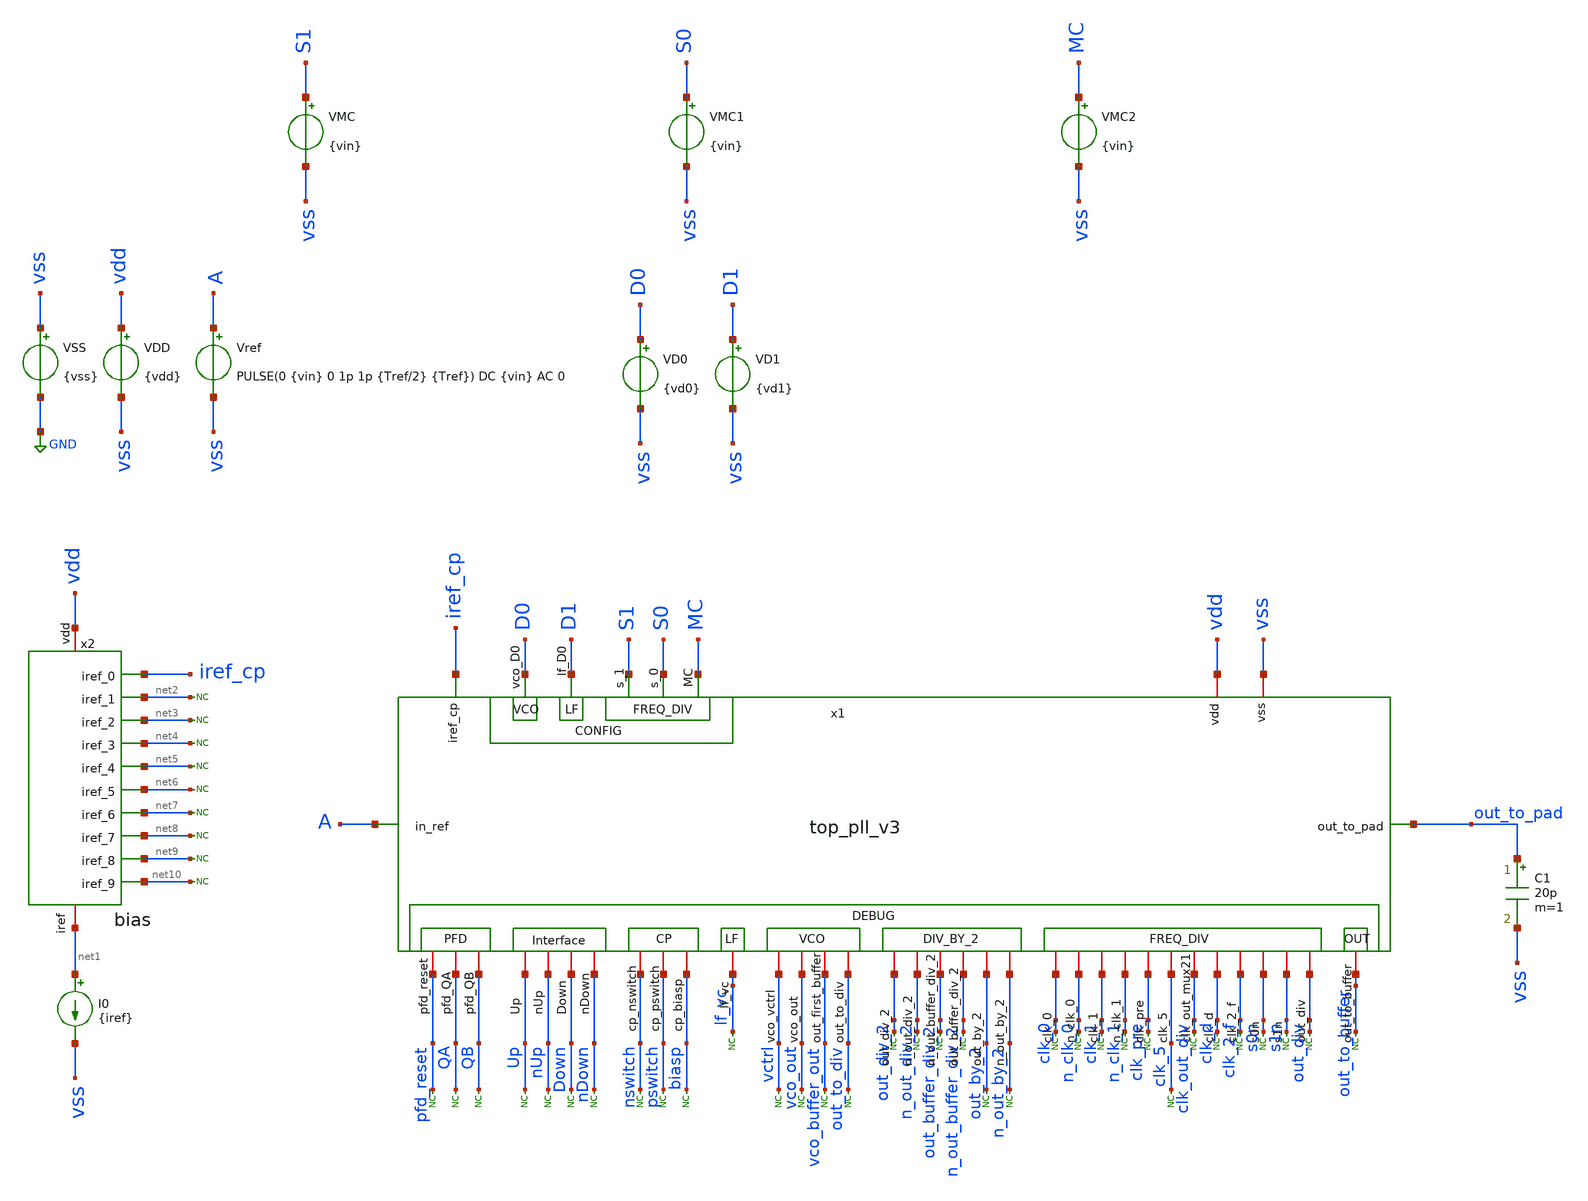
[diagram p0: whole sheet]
** sch_path: xschem/tb_top_pll_v3.sch
**.subckt tb_top_pll_v3
VSS vss GND {vss}
VDD vdd vss {vdd}
Vref A vss PULSE(0 {vin} 0 1p 1p {Tref/2} {Tref}) DC {vin} AC 0
VD0 D0 vss {vd0}
I0 net1 vss {iref}
* noconn #net2
* noconn #net3
* noconn #net4
* noconn #net5
* noconn #net6
* noconn #net7
* noconn #net8
* noconn #net9
* noconn #net10
* noconn clk_pre
* noconn n_clk_1
* noconn clk_1
* noconn n_clk_0
* noconn clk_0
* noconn n_out_buffer_div_2
* noconn out_buffer_div_2
* noconn n_out_div_2
* noconn out_div_2
* noconn nswitch
* noconn pswitch
* noconn biasp
* noconn pfd_reset
* noconn QA
* noconn QB
* noconn Up
* noconn nUp
* noconn Down
* noconn nDown
* noconn lf_vc
* noconn vctrl
* noconn vco_out
* noconn vco_buffer_out
* noconn out_to_div
* noconn out_by_2
* noconn n_out_by_2
* noconn clk_5
x2 vdd net1 iref_cp net2 net3 net4 net5 net6 net7 net8 net9 net10 bias
C1 out_to_pad vss 20p m=1
* noconn out_to_buffer
x1 iref_cp vss vdd vco_out vctrl Up QA out_to_buffer A nUp out_to_pad Down nDown QB D0 lf_vc
+ vco_buffer_out biasp pswitch nswitch pfd_reset S0 MC S1 out_by_2 out_to_div out_div n_out_by_2 n_out_div_2
+ out_div_2 out_buffer_div_2 n_out_buffer_div_2 n_clk_0 s1n s0n clk_2_f clk_d clk_out_div clk_5 clk_pre n_clk_1
+ clk_1 clk_0 D1 top_pll_v3
* noconn clk_out_div
* noconn clk_d
* noconn clk_2_f
* noconn s0n
* noconn s1n
* noconn out_div
VD1 D1 vss {vd1}
VMC S1 vss {vin}
VMC1 S0 vss {vin}
VMC2 MC vss {vin}
**** begin user architecture code



* Parameters
.param kp = 1.0
.param vdd = kp*1.8
.param vss = 0.0
.param vin = vdd
.param fref = 100e6
.param Tref = 1/fref
.param iref = 100u
.param vd0 = 0.0
.param vd1 = 0.0

.options TEMP = 100.0
.options RSHUNT = 1e20
.options GMIN = 1e-10

* Models
.lib ~/skywater/skywater-pdk/libraries/sky130_fd_pr_ngspice/latest/models/corners/sky130.lib SS

* Data to save

.ic v(A) = 0.0
.ic v(QA) = 0.0
.ic v(QB) = 0.0
.ic v(Up) = 0.0
.ic v(nUp) = 0.0
.ic v(Down) = 0.0
.ic v(nDown) = 0.0
.ic v(vctrl) = 0.0
.ic v(D0) = 0.0
.ic v(vco_out) = 0.0
.ic v(vco_buffer_out) = 0.0
.ic v(out_to_div) = 0.0
.ic v(out_to_pad) = 0.0
.ic v(out_div_2) = 0.0
.ic v(n_out_div_2) = 0.0
.ic v(out_buffer_div_2) = 0.0
.ic v(n_out_buffer_div_2) = 0.0
.ic v(out_by_2) = 0.0
.ic v(n_out_by_2) = 0.0
.ic v(clk_0) = 0.0
.ic v(n_clk_0) = 0.0
.ic v(clk_1) = 0.0
.ic v(n_clk_1) = 0.0
.ic v(clk_pre) = 0.0
.ic v(clk_5) = 0.0
.ic v(clk_d) = 0.0
.ic v(clk_2_f) = 0.0
.ic v(s1n) = 0.0
.ic v(s0n) = 0.0
.ic v(out_div) = 0.0


* Simulation
.control
	tran 0.01ns 1.5us
	meas tran Tosc trig v(out_to_pad) val=0.9 fall=1005 targ v(out_to_pad) val=0.9 fall=1105
	let  T = wTosc/100.0
	let  f = 1/T
	echo .
	echo ------ PLL simulation ------
	print T f
	*write tb_PLL_tran.raw
	plot v(vctrl) v(pfd_reset)+2 v(nDown)+4 v(Down)+6 v(nUp)+8 v(Up)+10 v(QA)+12 v(QB)+12 v(A)+14
+ v(out_div)+16
 	plot v(out_to_pad)+12 v(out_to_buffer)+9 v(out_to_div)+6 v(out_by_2)+3 v(out_div)
	plot v(out_div) v(out_by_2) v(out_to_div)
	plot v(vctrl)
	plot v(pswitch) v(nswitch) xlimit 1.4us 1.444us
.endc

.end


**** end user architecture code
**.ends
.GLOBAL GND
**** begin user architecture code
[sky130_models]
**** end user architecture code
.end
